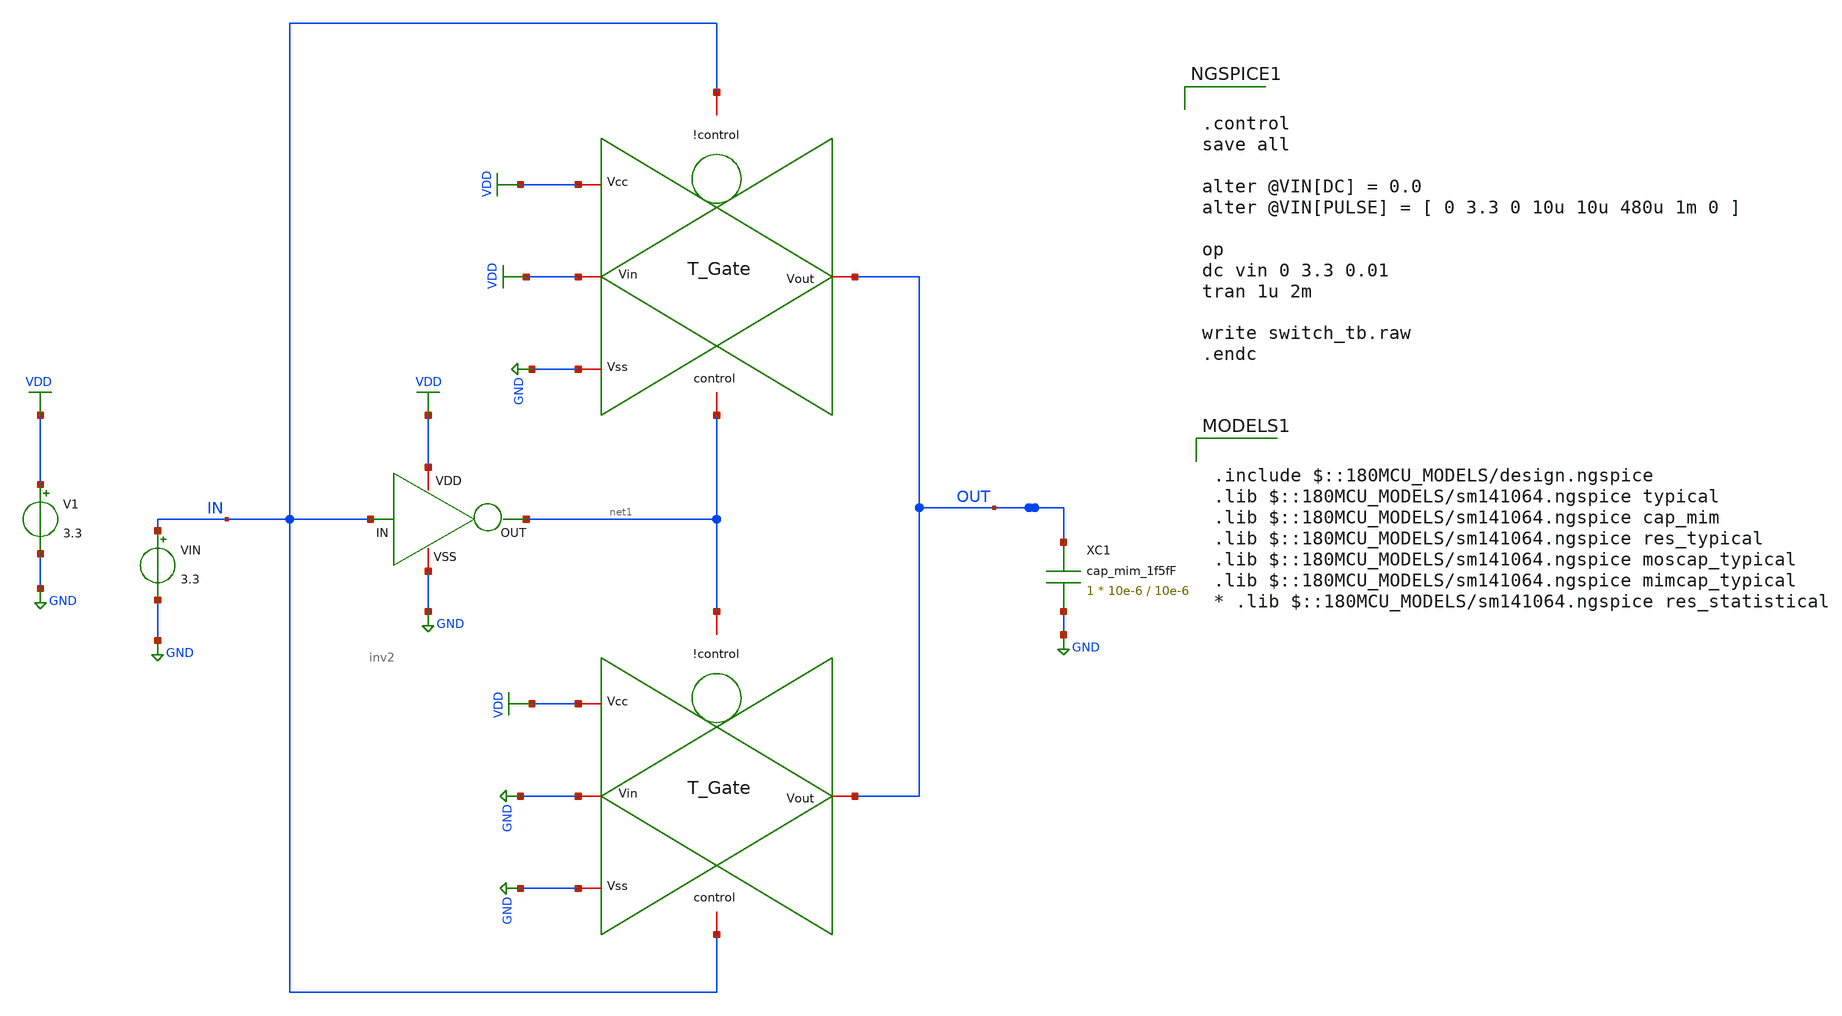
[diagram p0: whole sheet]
** sch_path: Array Components/Switch Array/switch_tb.sch
**.subckt switch_tb
x1 VDD IN net1 GND inv2
x2 IN VDD VDD OUT GND net1 T_gate
x3 net1 VDD GND OUT GND IN T_gate
V1 VDD GND 3.3
VIN IN GND 3.3
XC1 OUT GND cap_mim_1f5fF c_width=10e-6 c_length=10e-6 m=1
**** begin user architecture code


.control
save all

alter @VIN[DC] = 0.0
alter @VIN[PULSE] = [ 0 3.3 0 10u 10u 480u 1m 0 ]

op
dc vin 0 3.3 0.01
tran 1u 2m

write switch_tb.raw
.endc



.include $::180MCU_MODELS/design.ngspice
.lib $::180MCU_MODELS/sm141064.ngspice typical
.lib $::180MCU_MODELS/sm141064.ngspice cap_mim
.lib $::180MCU_MODELS/sm141064.ngspice res_typical
.lib $::180MCU_MODELS/sm141064.ngspice moscap_typical
.lib $::180MCU_MODELS/sm141064.ngspice mimcap_typical
* .lib $::180MCU_MODELS/sm141064.ngspice res_statistical

**** end user architecture code
**.ends

* expanding   symbol:  SAR ADC project/inv2.sym # of pins=4
** sym_path: Array Components/Switch Array/CMOS Inverter/inv2.sym
** sch_path: Array Components/Switch Array/CMOS Inverter/inv2.sch
.subckt inv2 VDD IN OUT VSS
*.iopin VDD
*.iopin VSS
*.ipin IN
*.opin OUT
XM1 OUT IN VSS VSS nfet_03v3 L=0.36u W=2u nf=1 ad='int((nf+1)/2) * W/nf * 0.18u' as='int((nf+2)/2) * W/nf * 0.18u'
+ pd='2*int((nf+1)/2) * (W/nf + 0.18u)' ps='2*int((nf+2)/2) * (W/nf + 0.18u)' nrd='0.18u / W' nrs='0.18u / W'
+ sa=0 sb=0 sd=0 m=1
XM2 OUT IN VDD VDD pfet_03v3 L=0.36u W=5u nf=1 ad='int((nf+1)/2) * W/nf * 0.18u' as='int((nf+2)/2) * W/nf * 0.18u'
+ pd='2*int((nf+1)/2) * (W/nf + 0.18u)' ps='2*int((nf+2)/2) * (W/nf + 0.18u)' nrd='0.18u / W' nrs='0.18u / W'
+ sa=0 sb=0 sd=0 m=1
.ends


* expanding   symbol:  SAR ADC project/T_gate.sym # of pins=6
** sym_path: Array Components/Switch Array/T Gate/T_gate.sym
** sch_path: Array Components/Switch Array/T Gate/T_gate.sch
.subckt T_gate !control Vcc Vin Vout Vss control
*.iopin Vout
*.iopin Vin
*.iopin !control
*.iopin control
*.iopin Vss
*.iopin Vcc
XM1 Vin control Vout Vss nfet_03v3 L=0.36u W=10u nf=1 ad='int((nf+1)/2) * W/nf * 0.18u' as='int((nf+2)/2) * W/nf * 0.18u'
+ pd='2*int((nf+1)/2) * (W/nf + 0.18u)' ps='2*int((nf+2)/2) * (W/nf + 0.18u)' nrd='0.18u / W' nrs='0.18u / W'
+ sa=0 sb=0 sd=0 m=1
XM2 Vin !control Vout Vcc pfet_03v3 L=0.36u W=35u nf=1 ad='int((nf+1)/2) * W/nf * 0.18u' as='int((nf+2)/2) * W/nf * 0.18u'
+ pd='2*int((nf+1)/2) * (W/nf + 0.18u)' ps='2*int((nf+2)/2) * (W/nf + 0.18u)' nrd='0.18u / W' nrs='0.18u / W'
+ sa=0 sb=0 sd=0 m=1
.ends

.GLOBAL GND
.GLOBAL VDD
.end
